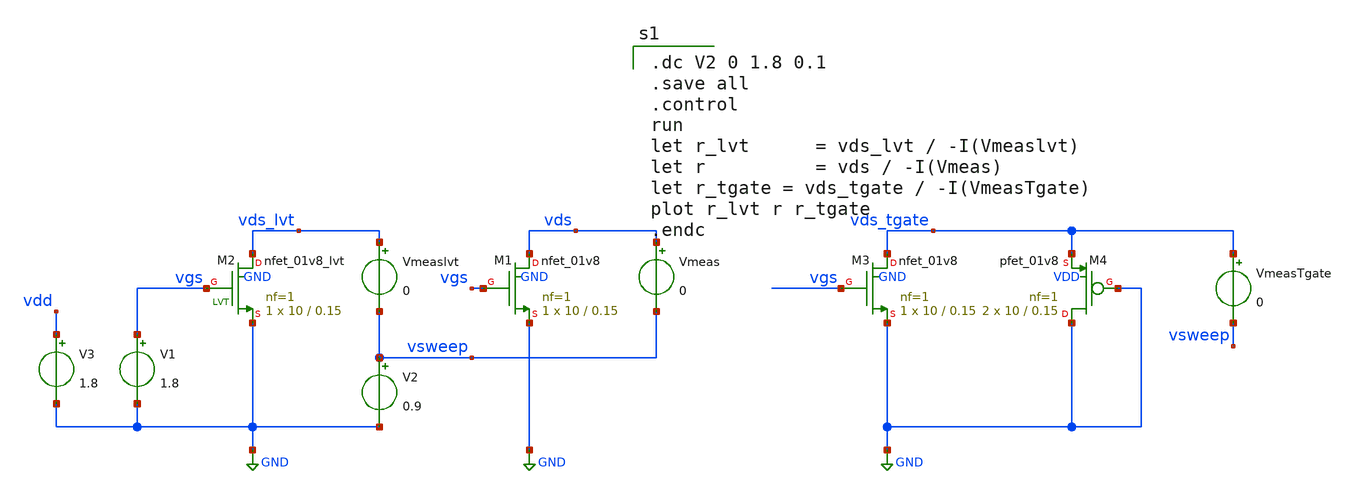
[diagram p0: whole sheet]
** sch_path: xschem/ztest.sch
**.subckt ztest
V1 vgs GND 1.8
V2 vsweep GND 0.9
XM1 vds vgs GND GND sky130_fd_pr__nfet_01v8 L=0.15 W=10 nf=1 ad='int((nf+1)/2) * W/nf * 0.29' as='int((nf+2)/2) * W/nf * 0.29'
+ pd='2*int((nf+1)/2) * (W/nf + 0.29)' ps='2*int((nf+2)/2) * (W/nf + 0.29)' nrd='0.29 / W' nrs='0.29 / W'
+ sa=0 sb=0 sd=0 mult=1 m=1
XM2 vds_lvt vgs GND GND sky130_fd_pr__nfet_01v8_lvt L=0.15 W=10 nf=1 ad='int((nf+1)/2) * W/nf * 0.29'
+ as='int((nf+2)/2) * W/nf * 0.29' pd='2*int((nf+1)/2) * (W/nf + 0.29)' ps='2*int((nf+2)/2) * (W/nf + 0.29)'
+ nrd='0.29 / W' nrs='0.29 / W' sa=0 sb=0 sd=0 mult=1 m=1
Vmeaslvt vds_lvt vsweep 0
Vmeas vds vsweep 0
VmeasTgate vds_tgate vsweep 0
V3 vdd GND 1.8
XM3 vds_tgate vgs GND GND sky130_fd_pr__nfet_01v8 L=0.15 W=10 nf=1 ad='int((nf+1)/2) * W/nf * 0.29' as='int((nf+2)/2) * W/nf * 0.29'
+ pd='2*int((nf+1)/2) * (W/nf + 0.29)' ps='2*int((nf+2)/2) * (W/nf + 0.29)' nrd='0.29 / W' nrs='0.29 / W'
+ sa=0 sb=0 sd=0 mult=1 m=1
XM4 GND GND vds_tgate VDD sky130_fd_pr__pfet_01v8 L=0.15 W=10 nf=1 ad='int((nf+1)/2) * W/nf * 0.29' as='int((nf+2)/2) * W/nf * 0.29'
+ pd='2*int((nf+1)/2) * (W/nf + 0.29)' ps='2*int((nf+2)/2) * (W/nf + 0.29)' nrd='0.29 / W' nrs='0.29 / W'
+ sa=0 sb=0 sd=0 mult=2 m=2
**** begin user architecture code
.lib $::SKYWATER_MODELS/sky130.lib.spice tt
.include $::PDKPATH/libs.ref/sky130_fd_sc_hs/spice/sky130_fd_sc_hs.spice


.dc V2 0 1.8 0.1
.save all
.control
run
let r_lvt      = vds_lvt / -I(Vmeaslvt)
let r          = vds / -I(Vmeas)
let r_tgate = vds_tgate / -I(VmeasTgate)
plot r_lvt r r_tgate
.endc


**** end user architecture code
**.ends
.GLOBAL GND
.end
